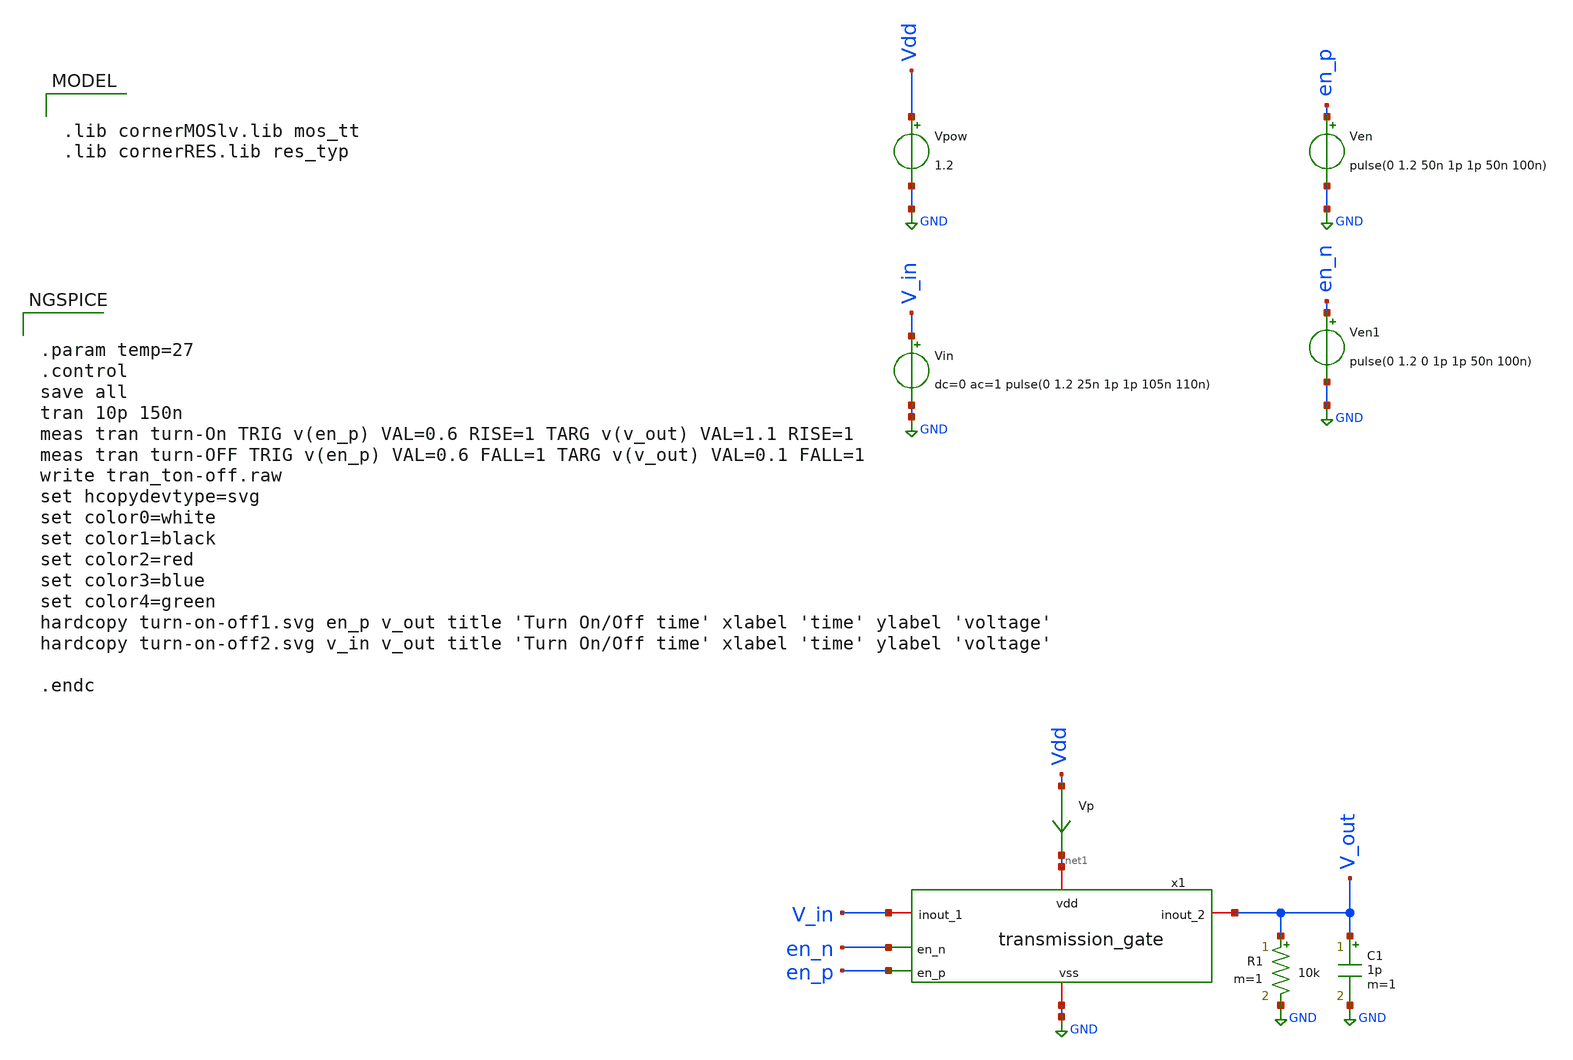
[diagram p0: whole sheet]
** sch_path: CHIPCHILE_CANELOS24_WorkshopTO/design_data/xschem/tgate/transmission_gate_tb_On-Off-time.sch
* Copyright 2023 IHP PDK Authors
**.subckt transmission_gate_tb_On-Off-time
Vpow Vdd GND 1.2
Vp Vdd net1 0
.save i(vp)
Vin V_in GND dc=0 ac=1 pulse(0 1.2 25n 1p 1p 105n 110n)
Ven en_p GND pulse(0 1.2 50n 1p 1p 50n 100n)
C1 V_out GND 1p m=1
Ven1 en_n GND pulse(0 1.2 0 1p 1p 50n 100n)
x1 net1 en_n V_in V_out en_p GND transmission_gate
R1 V_out GND 10k m=1
**** begin user architecture code

.lib cornerMOSlv.lib mos_tt
.lib cornerRES.lib res_typ



.param temp=27
.control
save all
tran 10p 150n
meas tran turn-On TRIG v(en_p) VAL=0.6 RISE=1 TARG v(v_out) VAL=1.1 RISE=1
meas tran turn-OFF TRIG v(en_p) VAL=0.6 FALL=1 TARG v(v_out) VAL=0.1 FALL=1
write tran_ton-off.raw
set hcopydevtype=svg
set color0=white
set color1=black
set color2=red
set color3=blue
set color4=green
hardcopy turn-on-off1.svg en_p v_out title 'Turn On/Off time' xlabel 'time' ylabel 'voltage'
hardcopy turn-on-off2.svg v_in v_out title 'Turn On/Off time' xlabel 'time' ylabel 'voltage'

.endc


**** end user architecture code
**.ends

* expanding   symbol:  transmission_gate.sym # of pins=6
** sym_path: CHIPCHILE_CANELOS24_WorkshopTO/design_data/xschem/multiplexer/transmission_gate.sym
** sch_path: CHIPCHILE_CANELOS24_WorkshopTO/design_data/xschem/multiplexer/transmission_gate.sch
.subckt transmission_gate vdd en_n inout_1 inout_2 en_p vss
*.iopin inout_1
*.iopin inout_2
*.ipin en_p
*.iopin vdd
*.iopin vss
*.ipin en_n
XM1 inout_1 en_p inout_2 net1 sg13_lv_nmos w=200.0u l=0.130u ng=20 m=1 mm_ok=1
XM2 inout_1 en_n inout_2 net2 sg13_lv_pmos w=200.0u l=0.130u ng=20 m=1 mm_ok=1
XR1 vdd net2 ntap1 R=262.8 w=0.78e-6 l=0.78e-6
XR2 vss net1 ptap1 R=262.8 w=0.78e-6 l=0.78e-6
.ends

.GLOBAL GND
.end
